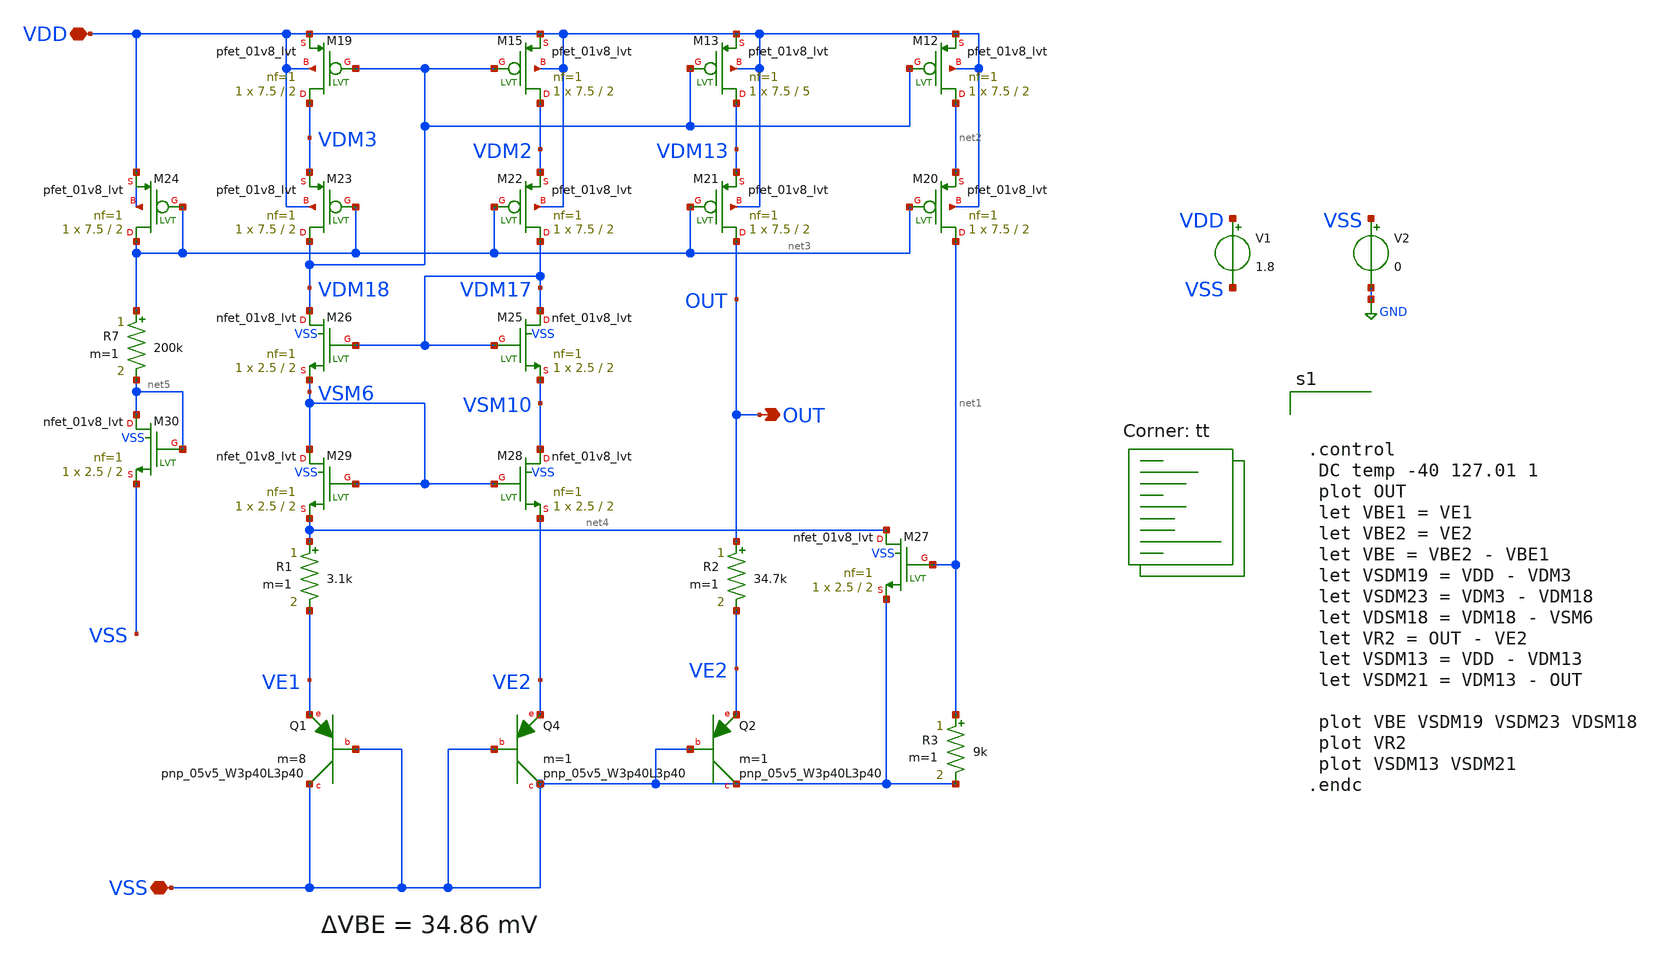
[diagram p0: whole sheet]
** sch_path: bgr-debug.sch
**.subckt bgr-debug VSS VDD OUT
*.iopin VSS
*.iopin VDD
*.opin OUT
V1 VDD VSS 1.8
V2 VSS GND 0
R3 net1 VSS 9k m=1
XQ4 VSS VSS VE2 sky130_fd_pr__pnp_05v5_W3p40L3p40 m=1
XQ1 VSS VSS VE1 sky130_fd_pr__pnp_05v5_W3p40L3p40 m=8
XQ2 VSS VSS VE2 sky130_fd_pr__pnp_05v5_W3p40L3p40 m=1
XM12 net2 VDM18 VDD VDD sky130_fd_pr__pfet_01v8_lvt L=2 W=7.5 nf=1 ad='int((nf+1)/2) * W/nf * 0.29' as='int((nf+2)/2) * W/nf * 0.29'
+ pd='2*int((nf+1)/2) * (W/nf + 0.29)' ps='2*int((nf+2)/2) * (W/nf + 0.29)' nrd='0.29 / W' nrs='0.29 / W'
+ sa=0 sb=0 sd=0 mult=1 m=1
XM13 VDM13 VDM18 VDD VDD sky130_fd_pr__pfet_01v8_lvt L=5 W=7.5 nf=1 ad='int((nf+1)/2) * W/nf * 0.29'
+ as='int((nf+2)/2) * W/nf * 0.29' pd='2*int((nf+1)/2) * (W/nf + 0.29)' ps='2*int((nf+2)/2) * (W/nf + 0.29)'
+ nrd='0.29 / W' nrs='0.29 / W' sa=0 sb=0 sd=0 mult=1 m=1
XM15 VDM2 VDM18 VDD VDD sky130_fd_pr__pfet_01v8_lvt L=2 W=7.5 nf=1 ad='int((nf+1)/2) * W/nf * 0.29' as='int((nf+2)/2) * W/nf * 0.29'
+ pd='2*int((nf+1)/2) * (W/nf + 0.29)' ps='2*int((nf+2)/2) * (W/nf + 0.29)' nrd='0.29 / W' nrs='0.29 / W'
+ sa=0 sb=0 sd=0 mult=1 m=1
XM19 VDM3 VDM18 VDD VDD sky130_fd_pr__pfet_01v8_lvt L=2 W=7.5 nf=1 ad='int((nf+1)/2) * W/nf * 0.29' as='int((nf+2)/2) * W/nf * 0.29'
+ pd='2*int((nf+1)/2) * (W/nf + 0.29)' ps='2*int((nf+2)/2) * (W/nf + 0.29)' nrd='0.29 / W' nrs='0.29 / W'
+ sa=0 sb=0 sd=0 mult=1 m=1
XM20 net1 net3 net2 VDD sky130_fd_pr__pfet_01v8_lvt L=2 W=7.5 nf=1 ad='int((nf+1)/2) * W/nf * 0.29' as='int((nf+2)/2) * W/nf * 0.29'
+ pd='2*int((nf+1)/2) * (W/nf + 0.29)' ps='2*int((nf+2)/2) * (W/nf + 0.29)' nrd='0.29 / W' nrs='0.29 / W'
+ sa=0 sb=0 sd=0 mult=1 m=1
XM21 OUT net3 VDM13 VDD sky130_fd_pr__pfet_01v8_lvt L=2 W=7.5 nf=1 ad='int((nf+1)/2) * W/nf * 0.29' as='int((nf+2)/2) * W/nf * 0.29'
+ pd='2*int((nf+1)/2) * (W/nf + 0.29)' ps='2*int((nf+2)/2) * (W/nf + 0.29)' nrd='0.29 / W' nrs='0.29 / W'
+ sa=0 sb=0 sd=0 mult=1 m=1
XM22 VDM17 net3 VDM2 VDD sky130_fd_pr__pfet_01v8_lvt L=2 W=7.5 nf=1 ad='int((nf+1)/2) * W/nf * 0.29'
+ as='int((nf+2)/2) * W/nf * 0.29' pd='2*int((nf+1)/2) * (W/nf + 0.29)' ps='2*int((nf+2)/2) * (W/nf + 0.29)'
+ nrd='0.29 / W' nrs='0.29 / W' sa=0 sb=0 sd=0 mult=1 m=1
XM23 VDM18 net3 VDM3 VDD sky130_fd_pr__pfet_01v8_lvt L=2 W=7.5 nf=1 ad='int((nf+1)/2) * W/nf * 0.29'
+ as='int((nf+2)/2) * W/nf * 0.29' pd='2*int((nf+1)/2) * (W/nf + 0.29)' ps='2*int((nf+2)/2) * (W/nf + 0.29)'
+ nrd='0.29 / W' nrs='0.29 / W' sa=0 sb=0 sd=0 mult=1 m=1
XM24 net3 net3 VDD VDD sky130_fd_pr__pfet_01v8_lvt L=2 W=7.5 nf=1 ad='int((nf+1)/2) * W/nf * 0.29' as='int((nf+2)/2) * W/nf * 0.29'
+ pd='2*int((nf+1)/2) * (W/nf + 0.29)' ps='2*int((nf+2)/2) * (W/nf + 0.29)' nrd='0.29 / W' nrs='0.29 / W'
+ sa=0 sb=0 sd=0 mult=1 m=1
XM25 VDM17 VDM17 VSM10 VSS sky130_fd_pr__nfet_01v8_lvt L=2 W=2.5 nf=1 ad='int((nf+1)/2) * W/nf * 0.29'
+ as='int((nf+2)/2) * W/nf * 0.29' pd='2*int((nf+1)/2) * (W/nf + 0.29)' ps='2*int((nf+2)/2) * (W/nf + 0.29)'
+ nrd='0.29 / W' nrs='0.29 / W' sa=0 sb=0 sd=0 mult=1 m=1
XM26 VDM18 VDM17 VSM6 VSS sky130_fd_pr__nfet_01v8_lvt L=2 W=2.5 nf=1 ad='int((nf+1)/2) * W/nf * 0.29'
+ as='int((nf+2)/2) * W/nf * 0.29' pd='2*int((nf+1)/2) * (W/nf + 0.29)' ps='2*int((nf+2)/2) * (W/nf + 0.29)'
+ nrd='0.29 / W' nrs='0.29 / W' sa=0 sb=0 sd=0 mult=1 m=1
XM27 net4 net1 VSS VSS sky130_fd_pr__nfet_01v8_lvt L=2 W=2.5 nf=1 ad='int((nf+1)/2) * W/nf * 0.29' as='int((nf+2)/2) * W/nf * 0.29'
+ pd='2*int((nf+1)/2) * (W/nf + 0.29)' ps='2*int((nf+2)/2) * (W/nf + 0.29)' nrd='0.29 / W' nrs='0.29 / W'
+ sa=0 sb=0 sd=0 mult=1 m=1
XM28 VSM10 VSM6 VE2 VSS sky130_fd_pr__nfet_01v8_lvt L=2 W=2.5 nf=1 ad='int((nf+1)/2) * W/nf * 0.29' as='int((nf+2)/2) * W/nf * 0.29'
+ pd='2*int((nf+1)/2) * (W/nf + 0.29)' ps='2*int((nf+2)/2) * (W/nf + 0.29)' nrd='0.29 / W' nrs='0.29 / W'
+ sa=0 sb=0 sd=0 mult=1 m=1
XM29 VSM6 VSM6 net4 VSS sky130_fd_pr__nfet_01v8_lvt L=2 W=2.5 nf=1 ad='int((nf+1)/2) * W/nf * 0.29' as='int((nf+2)/2) * W/nf * 0.29'
+ pd='2*int((nf+1)/2) * (W/nf + 0.29)' ps='2*int((nf+2)/2) * (W/nf + 0.29)' nrd='0.29 / W' nrs='0.29 / W'
+ sa=0 sb=0 sd=0 mult=1 m=1
R7 net3 net5 200k m=1
XM30 net5 net5 VSS VSS sky130_fd_pr__nfet_01v8_lvt L=2 W=2.5 nf=1 ad='int((nf+1)/2) * W/nf * 0.29' as='int((nf+2)/2) * W/nf * 0.29'
+ pd='2*int((nf+1)/2) * (W/nf + 0.29)' ps='2*int((nf+2)/2) * (W/nf + 0.29)' nrd='0.29 / W' nrs='0.29 / W'
+ sa=0 sb=0 sd=0 mult=1 m=1
R1 net4 VE1 3.1k m=1
R2 OUT VE2 34.7k m=1
**** begin user architecture code
.lib $::SKYWATER_MODELS/sky130.lib.spice tt



.control
 DC temp -40 127.01 1
 plot OUT
 let VBE1 = VE1
 let VBE2 = VE2
 let VBE = VBE2 - VBE1
 let VSDM19 = VDD - VDM3
 let VSDM23 = VDM3 - VDM18
 let VDSM18 = VDM18 - VSM6
 let VR2 = OUT - VE2
 let VSDM13 = VDD - VDM13
 let VSDM21 = VDM13 - OUT

 plot VBE VSDM19 VSDM23 VDSM18
 plot VR2
 plot VSDM13 VSDM21
.endc


**** end user architecture code
**.ends
.GLOBAL GND
.end
